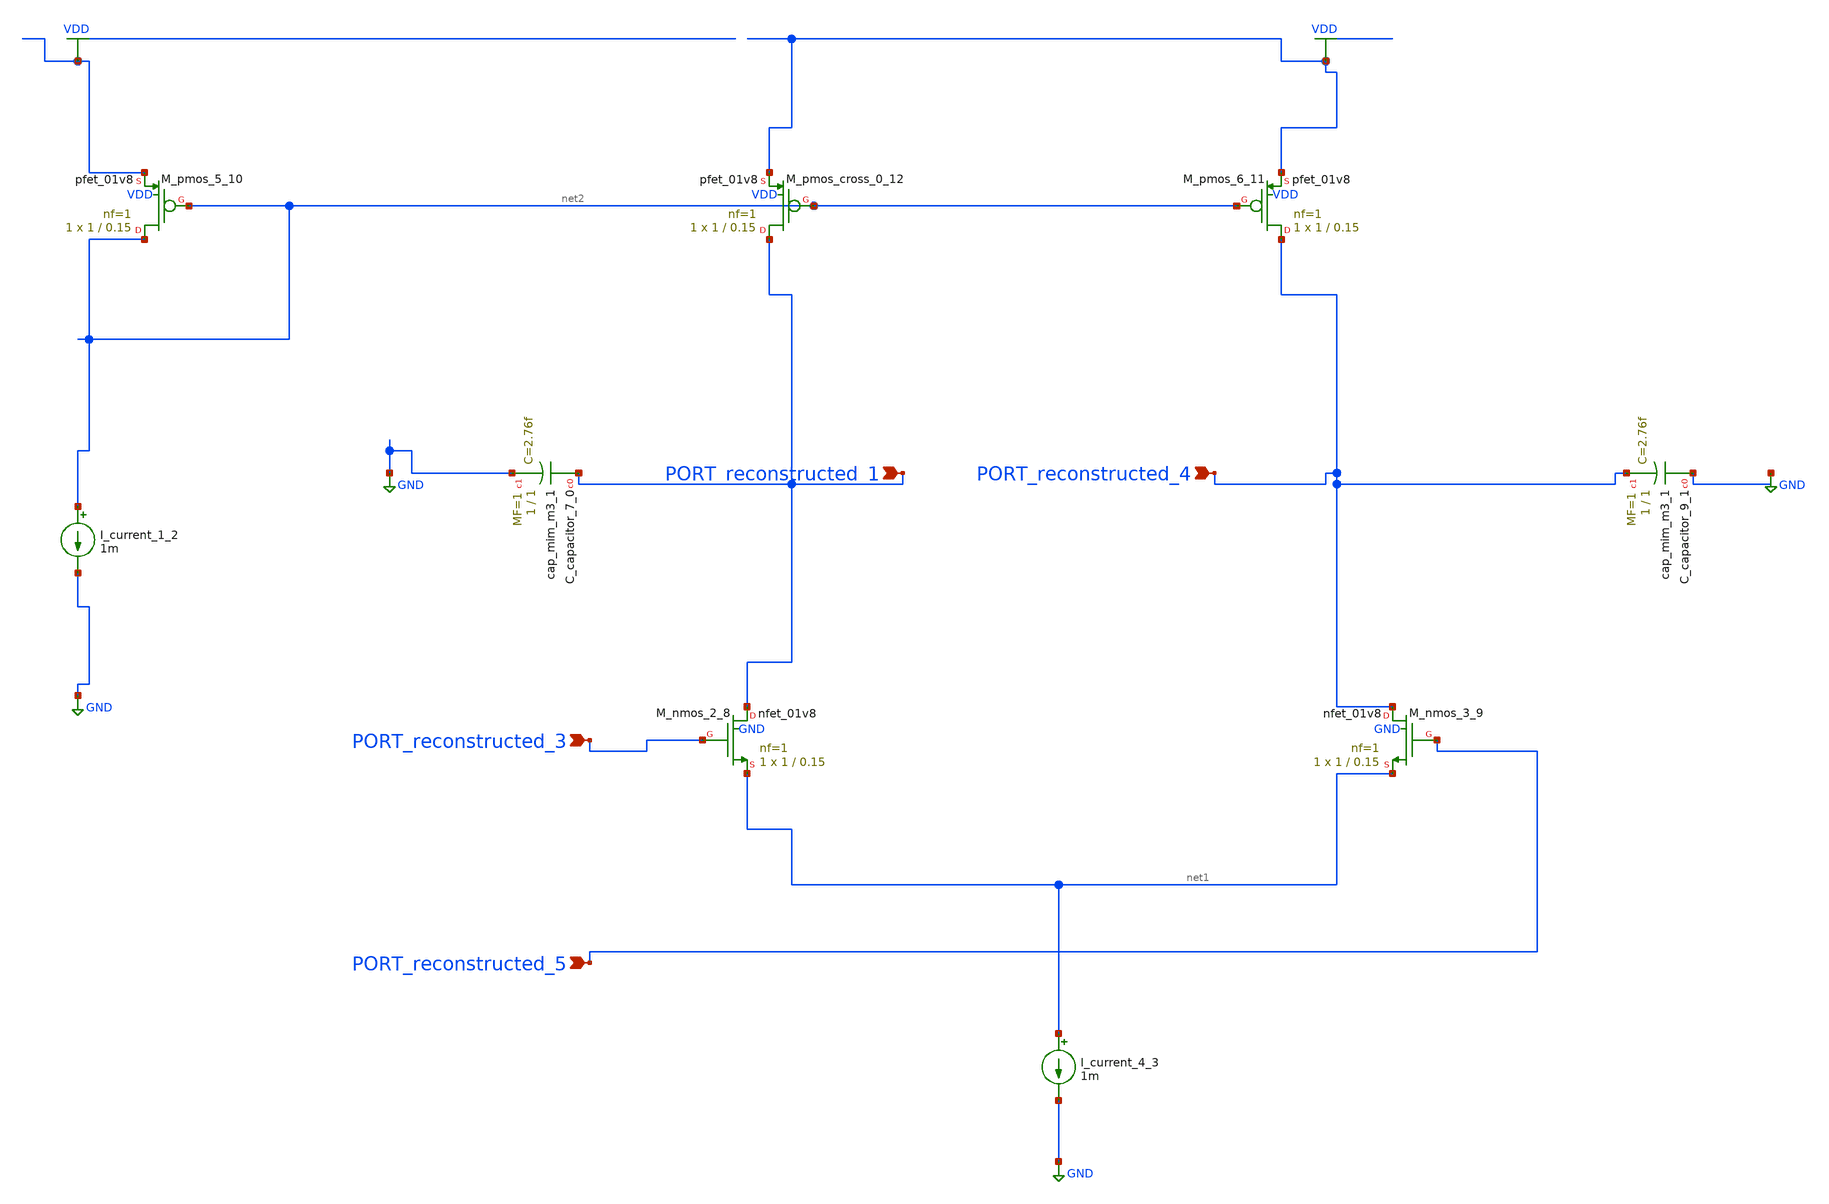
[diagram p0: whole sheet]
** sch_path: schematics/AMSNet/387.sch
**.subckt 387 PORT_reconstructed_4 PORT_reconstructed_1 PORT_reconstructed_3 PORT_reconstructed_5
*.ipin PORT_reconstructed_4
*.ipin PORT_reconstructed_1
*.ipin PORT_reconstructed_3
*.ipin PORT_reconstructed_5
XC_capacitor_7_0 PORT_reconstructed_1 GND sky130_fd_pr__cap_mim_m3_1 W=1 L=1 MF=1 m=1
XC_capacitor_9_1 GND PORT_reconstructed_4 sky130_fd_pr__cap_mim_m3_1 W=1 L=1 MF=1 m=1
I_current_1_2 net2 GND 1m
I_current_4_3 net1 GND 1m
XM_nmos_2_8 PORT_reconstructed_1 PORT_reconstructed_3 net1 GND sky130_fd_pr__nfet_01v8 L=0.15 W=1 nf=1
+ ad='int((1 + 1)/2) * 1 / 1 * 0.29' as='int((1 + 2)/2) * 1 / 1 * 0.29' pd='2*int((1 + 1)/2) * (1 / 1 + 0.29)'
+ ps='2*int((1 + 2)/2) * (1 / 1 + 0.29)' nrd='0.29 / 1 ' nrs='0.29 / 1 ' sa=0 sb=0 sd=0 mult=1 m=1
XM_nmos_3_9 PORT_reconstructed_4 PORT_reconstructed_5 net1 GND sky130_fd_pr__nfet_01v8 L=0.15 W=1 nf=1
+ ad='int((1 + 1)/2) * 1 / 1 * 0.29' as='int((1 + 2)/2) * 1 / 1 * 0.29' pd='2*int((1 + 1)/2) * (1 / 1 + 0.29)'
+ ps='2*int((1 + 2)/2) * (1 / 1 + 0.29)' nrd='0.29 / 1 ' nrs='0.29 / 1 ' sa=0 sb=0 sd=0 mult=1 m=1
XM_pmos_5_10 net2 net2 VDD VDD sky130_fd_pr__pfet_01v8 L=0.15 W=1 nf=1 ad='int((1 + 1)/2) * 1 / 1 * 0.29'
+ as='int((1 + 2)/2) * 1 / 1 * 0.29' pd='2*int((1 + 1)/2) * (1 / 1 + 0.29)' ps='2*int((1 + 2)/2) * (1 / 1 + 0.29)'
+ nrd='0.29 / 1 ' nrs='0.29 / 1 ' sa=0 sb=0 sd=0 mult=1 m=1
XM_pmos_6_11 PORT_reconstructed_4 net2 VDD VDD sky130_fd_pr__pfet_01v8 L=0.15 W=1 nf=1 ad='int((1 + 1)/2) * 1 / 1 * 0.29'
+ as='int((1 + 2)/2) * 1 / 1 * 0.29' pd='2*int((1 + 1)/2) * (1 / 1 + 0.29)' ps='2*int((1 + 2)/2) * (1 / 1 + 0.29)'
+ nrd='0.29 / 1 ' nrs='0.29 / 1 ' sa=0 sb=0 sd=0 mult=1 m=1
XM_pmos_cross_0_12 PORT_reconstructed_1 net2 VDD VDD sky130_fd_pr__pfet_01v8 L=0.15 W=1 nf=1 ad='int((1 + 1)/2) * 1 / 1 * 0.29'
+ as='int((1 + 2)/2) * 1 / 1 * 0.29' pd='2*int((1 + 1)/2) * (1 / 1 + 0.29)' ps='2*int((1 + 2)/2) * (1 / 1 + 0.29)'
+ nrd='0.29 / 1 ' nrs='0.29 / 1 ' sa=0 sb=0 sd=0 mult=1 m=1
**.ends
.GLOBAL GND
.GLOBAL VDD
.end
